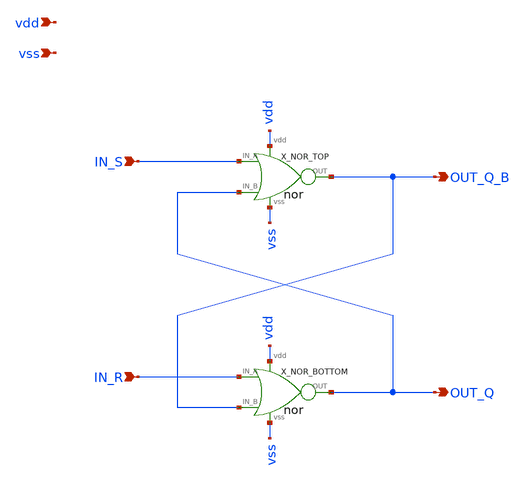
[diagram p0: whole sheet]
** sch_path: xsch/ip/logic/sr_latch.sch
**.subckt sr_latch IN_R OUT_Q_B OUT_Q IN_S vdd vss
*.ipin IN_R
*.opin OUT_Q_B
*.opin OUT_Q
*.ipin IN_S
*.ipin vdd
*.ipin vss
X_NOR_TOP IN_S OUT_Q_B vdd vss OUT_Q nor
X_NOR_BOTTOM IN_R OUT_Q vdd vss OUT_Q_B nor
**.ends

* expanding   symbol:  ip/logic/nor.sym # of pins=5
** sym_path: xsch/ip/logic/nor.sym
** sch_path: xsch/ip/logic/nor.sch
.subckt nor IN_A OUT vdd vss IN_B
*.ipin IN_A
*.opin OUT
*.iopin vss
*.iopin vdd
*.ipin IN_B
XMn_a OUT IN_A vss vss sky130_fd_pr__nfet_01v8 L=0.15 W=1 nf=1 ad='int((1 + 1)/2) * 1 / 1 * 0.29' as='int((1 + 2)/2) * 1 / 1 * 0.29'
+ pd='2*int((1 + 1)/2) * (1 / 1 + 0.29)' ps='2*int((1 + 2)/2) * (1 / 1 + 0.29)' nrd='0.29 / 1 ' nrs='0.29 / 1 '
+ sa=0 sb=0 sd=0 mult=1 m=1
XMp_a mpcon IN_A vdd vdd sky130_fd_pr__pfet_01v8 L=0.15 W=1 nf=2 ad='int((nf+1)/2) * W/nf * 0.29' as='int((nf+2)/2) * W/nf * 0.29'
+ pd='2*int((nf+1)/2) * (W/nf + 0.29)' ps='2*int((nf+2)/2) * (W/nf + 0.29)' nrd='0.29 / W' nrs='0.29 / W'
+ sa=0 sb=0 sd=0 mult=1 m=1
XMp_b OUT IN_B mpcon vdd sky130_fd_pr__pfet_01v8 L=0.15 W=1 nf=2 ad='int((nf+1)/2) * W/nf * 0.29' as='int((nf+2)/2) * W/nf * 0.29'
+ pd='2*int((nf+1)/2) * (W/nf + 0.29)' ps='2*int((nf+2)/2) * (W/nf + 0.29)' nrd='0.29 / W' nrs='0.29 / W'
+ sa=0 sb=0 sd=0 mult=1 m=1
XMn_b OUT IN_B vss vss sky130_fd_pr__nfet_01v8 L=0.15 W=1 nf=1 ad='int((1 + 1)/2) * 1 / 1 * 0.29' as='int((1 + 2)/2) * 1 / 1 * 0.29'
+ pd='2*int((1 + 1)/2) * (1 / 1 + 0.29)' ps='2*int((1 + 2)/2) * (1 / 1 + 0.29)' nrd='0.29 / 1 ' nrs='0.29 / 1 '
+ sa=0 sb=0 sd=0 mult=1 m=1
.ends

.end
